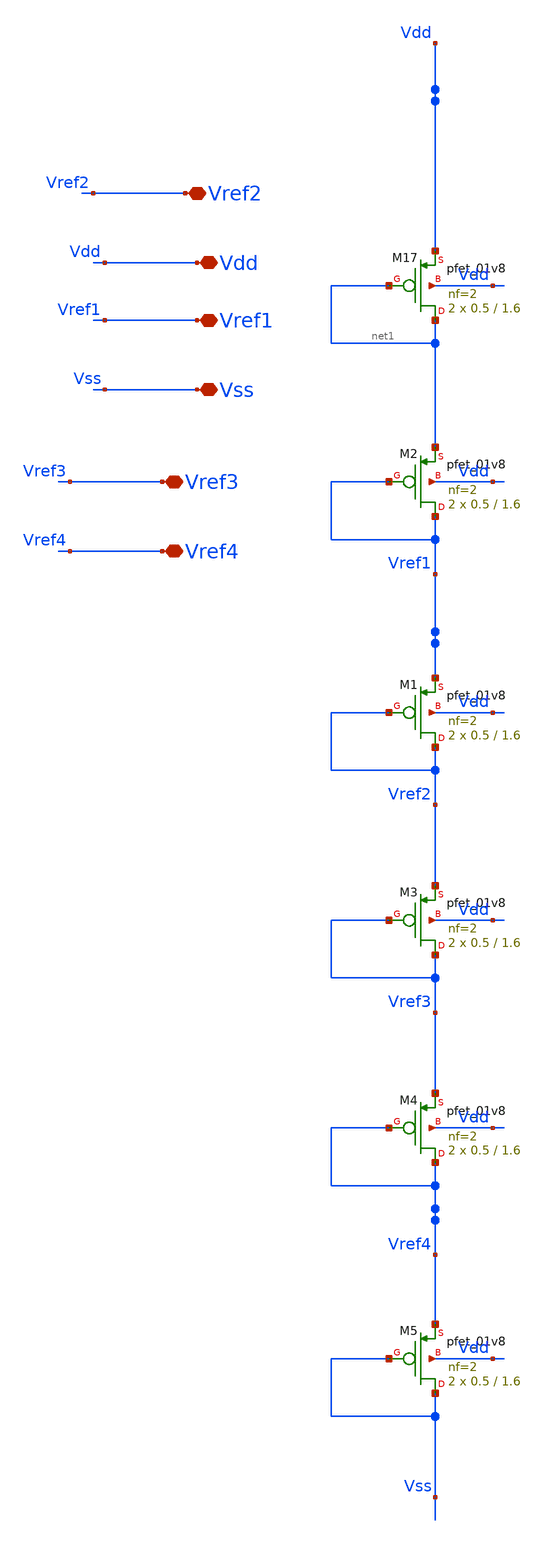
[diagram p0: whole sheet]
** sch_path: xschem/vol_ref_gen_tt.sch
**.subckt vol_ref_gen_tt Vdd Vref1 Vss Vref2 Vref3 Vref4
*.iopin Vdd
*.iopin Vref1
*.iopin Vss
*.iopin Vref2
*.iopin Vref3
*.iopin Vref4
XM17 net1 net1 Vdd Vdd sky130_fd_pr__pfet_01v8 L=1.6 W=0.5 nf=2 ad='int((nf+1)/2) * W/nf * 0.29' as='int((nf+2)/2) * W/nf * 0.29'
+ pd='2*int((nf+1)/2) * (W/nf + 0.29)' ps='2*int((nf+2)/2) * (W/nf + 0.29)' nrd='0.29 / W' nrs='0.29 / W'
+ sa=0 sb=0 sd=0 mult=2 m=2
XM2 Vref1 Vref1 net1 Vdd sky130_fd_pr__pfet_01v8 L=1.6 W=0.5 nf=2 ad='int((nf+1)/2) * W/nf * 0.29' as='int((nf+2)/2) * W/nf * 0.29'
+ pd='2*int((nf+1)/2) * (W/nf + 0.29)' ps='2*int((nf+2)/2) * (W/nf + 0.29)' nrd='0.29 / W' nrs='0.29 / W'
+ sa=0 sb=0 sd=0 mult=2 m=2
XM1 Vref2 Vref2 Vref1 Vdd sky130_fd_pr__pfet_01v8 L=1.6 W=0.5 nf=2 ad='int((nf+1)/2) * W/nf * 0.29' as='int((nf+2)/2) * W/nf * 0.29'
+ pd='2*int((nf+1)/2) * (W/nf + 0.29)' ps='2*int((nf+2)/2) * (W/nf + 0.29)' nrd='0.29 / W' nrs='0.29 / W'
+ sa=0 sb=0 sd=0 mult=2 m=2
XM3 Vref3 Vref3 Vref2 Vdd sky130_fd_pr__pfet_01v8 L=1.6 W=0.5 nf=2 ad='int((nf+1)/2) * W/nf * 0.29' as='int((nf+2)/2) * W/nf * 0.29'
+ pd='2*int((nf+1)/2) * (W/nf + 0.29)' ps='2*int((nf+2)/2) * (W/nf + 0.29)' nrd='0.29 / W' nrs='0.29 / W'
+ sa=0 sb=0 sd=0 mult=2 m=2
XM4 Vref4 Vref4 Vref3 Vdd sky130_fd_pr__pfet_01v8 L=1.6 W=0.5 nf=2 ad='int((nf+1)/2) * W/nf * 0.29' as='int((nf+2)/2) * W/nf * 0.29'
+ pd='2*int((nf+1)/2) * (W/nf + 0.29)' ps='2*int((nf+2)/2) * (W/nf + 0.29)' nrd='0.29 / W' nrs='0.29 / W'
+ sa=0 sb=0 sd=0 mult=2 m=2
XM5 Vss Vss Vref4 Vdd sky130_fd_pr__pfet_01v8 L=1.6 W=0.5 nf=2 ad='int((nf+1)/2) * W/nf * 0.29' as='int((nf+2)/2) * W/nf * 0.29'
+ pd='2*int((nf+1)/2) * (W/nf + 0.29)' ps='2*int((nf+2)/2) * (W/nf + 0.29)' nrd='0.29 / W' nrs='0.29 / W'
+ sa=0 sb=0 sd=0 mult=2 m=2
**.ends
.end
